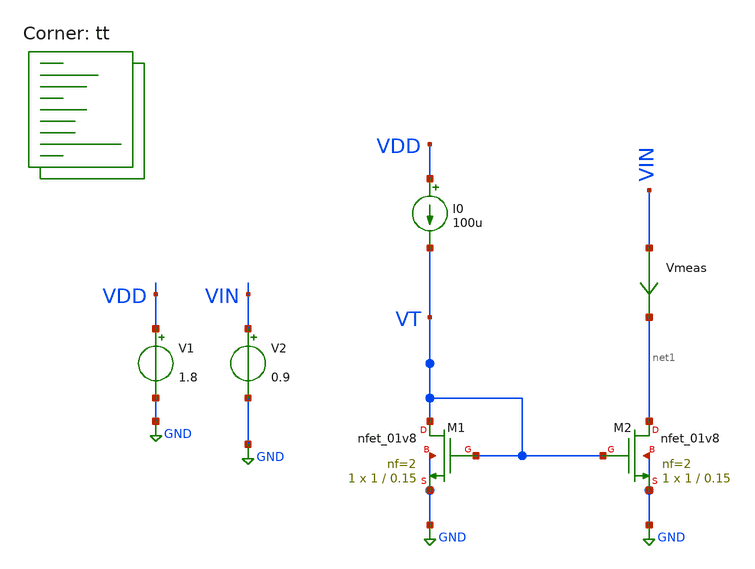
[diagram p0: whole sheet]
** sch_path: sky130B/Analog_integrated_circuit_Design/chapter3/4/4.sch
**.subckt 4
V1 VDD GND 1.8
V2 VIN GND 0.9
Vmeas VIN net1 0
.save i(vmeas)
XM1 VT VT GND GND sky130_fd_pr__nfet_01v8 L=0.15 W=1 nf=2 ad='int((2 + 1)/2) * 1 / 2 * 0.29' as='int((2 + 2)/2) * 1 / 2 * 0.29'
+ pd='2*int((2 + 1)/2) * (1 / 2 + 0.29)' ps='2*int((2 + 2)/2) * (1 / 2 + 0.29)' nrd='0.29 / 1 ' nrs='0.29 / 1 '
+ sa=0 sb=0 sd=0 mult=1 m=1
I0 VDD VT 100u
XM2 net1 VT GND GND sky130_fd_pr__nfet_01v8 L=0.15 W=1 nf=2 ad='int((2 + 1)/2) * 1 / 2 * 0.29' as='int((2 + 2)/2) * 1 / 2 * 0.29'
+ pd='2*int((2 + 1)/2) * (1 / 2 + 0.29)' ps='2*int((2 + 2)/2) * (1 / 2 + 0.29)' nrd='0.29 / 1 ' nrs='0.29 / 1 '
+ sa=0 sb=0 sd=0 mult=1 m=1
**** begin user architecture code
.lib $::SKYWATER_MODELS/sky130.lib.spice tt

**************************************************************
**************************************************************
**************************************************************
**************************************************************
**************************************************************
*LIBs*********************************************************
**************************************************************
**************************************************************
**************************************************************
**************************************************************
**************************************************************
*.lib $::SKYWATER_MODELS/sky130.lib.spice tt
* chose the corners in the corner file
* tt_mm for mismatch
* ss ff sf fs standart corners
* ll hh lh hl capacitor and resistors corners
* mc for total process variation including corners
**************************************************************
**************************************************************
**************************************************************
**************************************************************
**************************************************************
*Corners/montecarlo options***********************************
**************************************************************
**************************************************************
**************************************************************
**************************************************************
**************************************************************
.TEMP 27
**************************************************************
**************************************************************
**************************************************************
**************************************************************
*SIMULATION and Plots*****************************************
**************************************************************
**************************************************************
**************************************************************
**************************************************************
.control
save all
dc V2 0 1.8 0.001
*dc simulation
plot i(Vmeas)
plot v(VT)
plot 1/deriv(i(Vmeas))
.endc

**** end user architecture code
**.ends
.GLOBAL GND
.end
